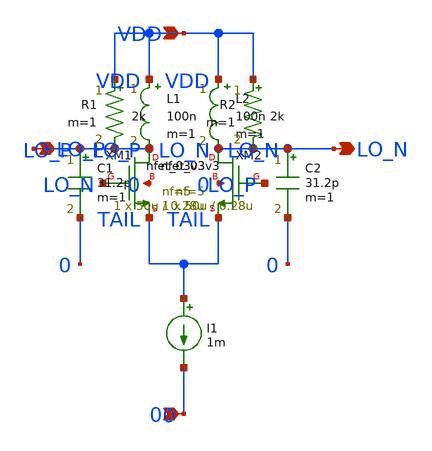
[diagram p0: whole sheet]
** sch_path: modules/PandaChip/designs/rf_trans/lo.sch
**.subckt lo VDD LO_P LO_N 0
*.ipin VDD
*.opin LO_P
*.opin LO_N
*.ipin 0
XM1 LO_P LO_N TAIL 0 nfet_03v3 L=0.28u W=50u nf=5 ad='int((nf+1)/2) * W/nf * 0.18u' as='int((nf+2)/2) * W/nf * 0.18u'
+ pd='2*int((nf+1)/2) * (W/nf + 0.18u)' ps='2*int((nf+2)/2) * (W/nf + 0.18u)' nrd='0.18u / W' nrs='0.18u / W'
+ sa=0 sb=0 sd=0 m=1
XM2 LO_N LO_P TAIL 0 nfet_03v3 L=0.28u W=50u nf=5 ad='int((nf+1)/2) * W/nf * 0.18u' as='int((nf+2)/2) * W/nf * 0.18u'
+ pd='2*int((nf+1)/2) * (W/nf + 0.18u)' ps='2*int((nf+2)/2) * (W/nf + 0.18u)' nrd='0.18u / W' nrs='0.18u / W'
+ sa=0 sb=0 sd=0 m=1
L1 VDD LO_P 100n m=1
L2 VDD LO_N 100n m=1
R1 VDD LO_P 2k m=1
R2 VDD LO_N 2k m=1
C1 LO_P 0 31.2p m=1
C2 LO_N 0 31.2p m=1
I1 TAIL 0 1m
**.ends
.end
